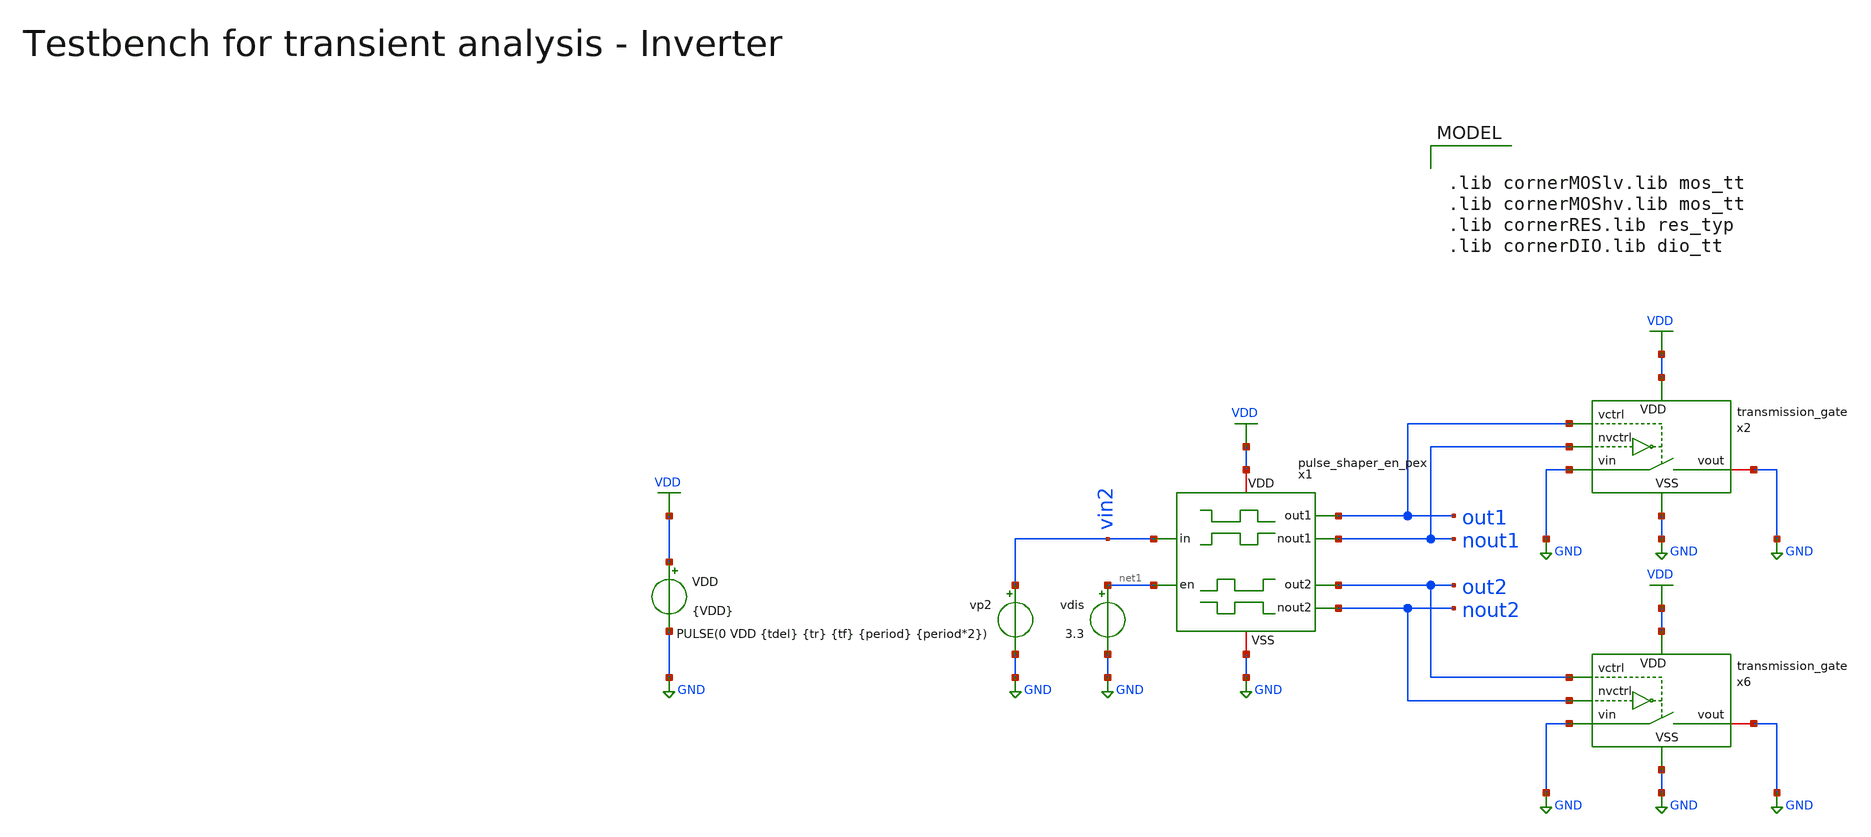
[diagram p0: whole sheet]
** sch_path: macros/heichips26_vcr/macros/switched_capacitor/testbenches/xschem/tb_pulse_shaper_en_pex_tran.sch
**.subckt tb_pulse_shaper_en_pex_tran
VDD VDD GND {VDD}
vp2 vin2 GND PULSE(0 VDD {tdel} {tr} {tf} {period} {period*2})
vdis net1 GND 3.3
x2 out1 GND GND nout1 VDD GND transmission_gate
x6 out2 GND GND nout2 VDD GND transmission_gate
x1 out1 nout1 VDD vin2 GND out2 nout2 net1 pulse_shaper_en_pex
**** begin user architecture code


.include ../../../netlist/pex/pulse_shaper_en_magic_pex_3.spice

.param VDD=3.3
.csparam VDD=VDD
.param Vcm=VDD/2
.param temp=27
.param Cload=10p
.param Rload=1k

.param period = 4n
.param tdel   = {period/2}
.param ton    = {period*2}
.csparam tstop  = {2.5*period}
.csparam tstep  = {period/100}
.param tr     = {period/100}
.param tf     = {period/100}

.options savecurrents klu method=gear reltol=1e-4 abstol=1e-15 gmin=1e-15
.control

save all

* Transient Analysis
tran {$&tstep} {$&tstop}
write @schname\.raw

* Plotting
plot vin2
plot out1+4 out2 nout1 nout2+4


*quit
.endc



.lib cornerMOSlv.lib mos_tt
.lib cornerMOShv.lib mos_tt
.lib cornerRES.lib res_typ
.lib cornerDIO.lib dio_tt

**** end user architecture code
**.ends

* expanding   symbol:  transmission_gate.sym # of pins=6
** sym_path: macros/heichips26_vcr/macros/switched_capacitor/schematic/xschem/transmission_gate.sym
** sch_path: macros/heichips26_vcr/macros/switched_capacitor/schematic/xschem/transmission_gate.sch
.subckt transmission_gate vctrl vin vout nvctrl VDD VSS
*.iopin vin
*.iopin vout
*.ipin vctrl
*.ipin nvctrl
*.iopin VDD
*.iopin VSS
XM3 vout vctrl vin VSS sg13_hv_nmos w={tg_ngate_w*tg_ng} l={tg_ch_len} ng={tg_ng} m=1 mm_ok=1
XM4 vout nvctrl vin VDD sg13_hv_pmos w={tg_pgate_w*tg_ng} l={tg_ch_len} ng={tg_ng} m=1 mm_ok=1
**** begin user architecture code


.param tg_ch_len=0.45u
.param tg_ngate_w=2u
.param tg_pgate_w=5u
.param tg_ng=20


**** end user architecture code
.ends

.GLOBAL GND
.GLOBAL VDD
.end
